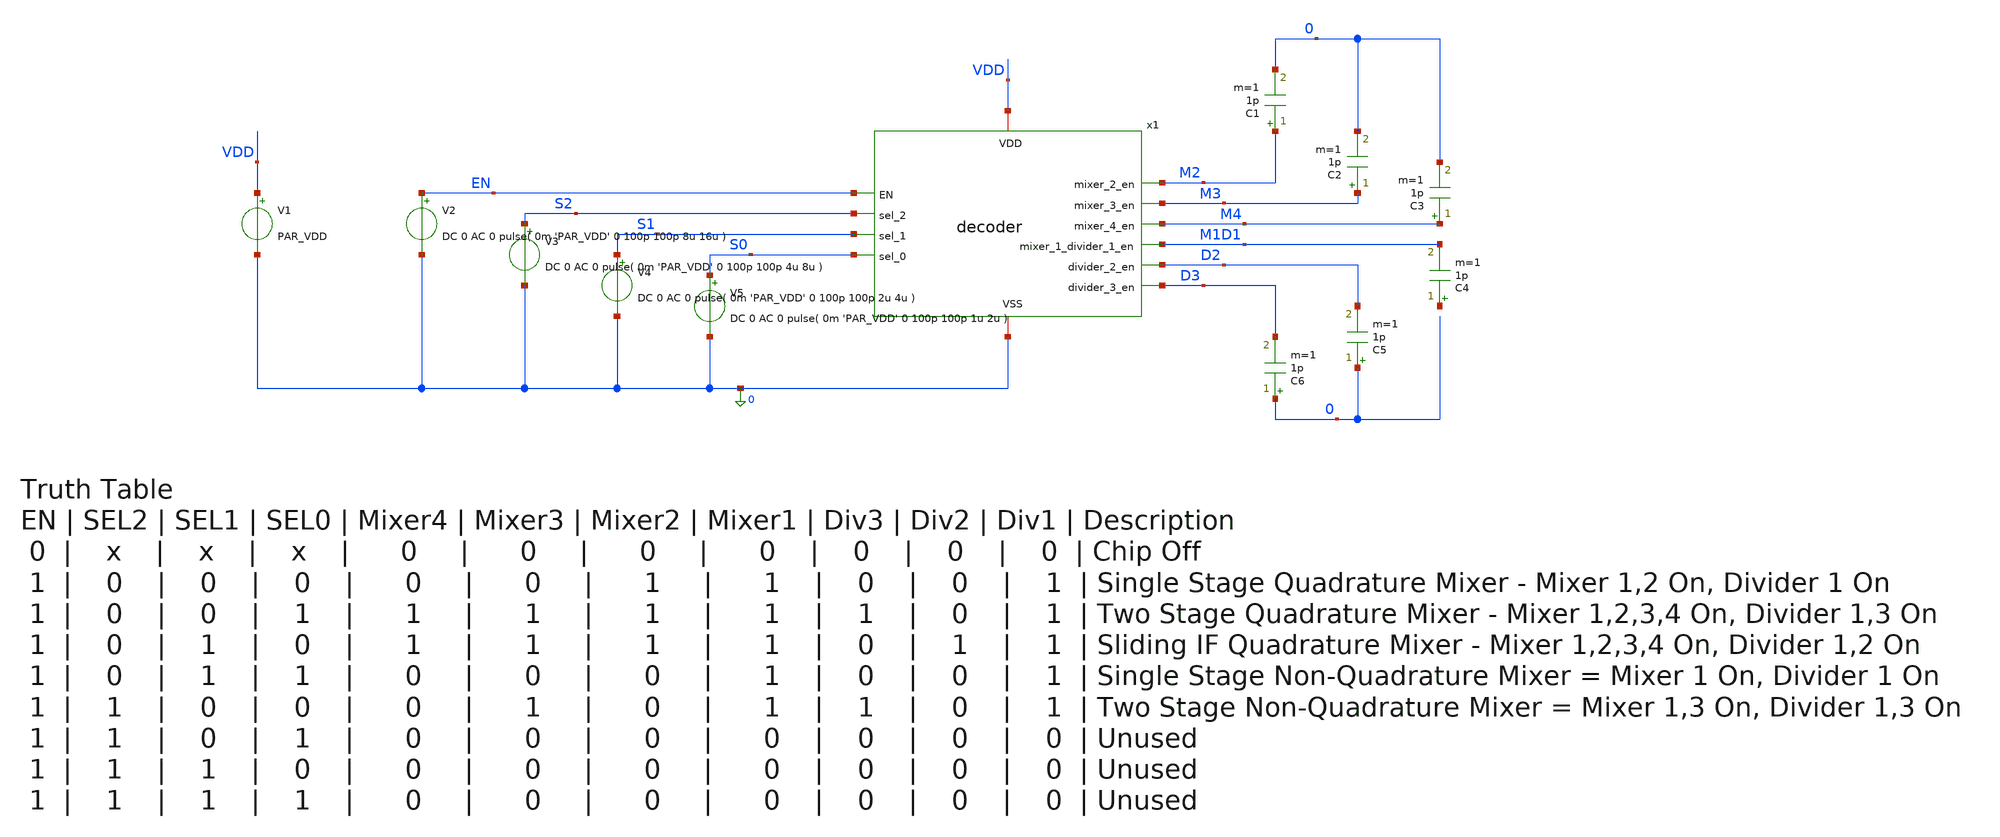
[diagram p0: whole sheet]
** sch_path: designs/decoder/testbench/tb_decoder.sch
**.subckt tb_decoder
C1 M2 0 1p m=1
C2 M3 0 1p m=1
C3 M4 0 1p m=1
C4 net1 M1D1 1p m=1
C5 0 D2 1p m=1
C6 0 D3 1p m=1
V1 VDD 0 PAR_VDD
V2 EN 0 DC 0 AC 0 pulse( 0m 'PAR_VDD' 0 100p 100p 8u 16u )
V3 S2 0 DC 0 AC 0 pulse( 0m 'PAR_VDD' 0 100p 100p 4u 8u )
V4 S1 0 DC 0 AC 0 pulse( 0m 'PAR_VDD' 0 100p 100p 2u 4u )
V5 S0 0 DC 0 AC 0 pulse( 0m 'PAR_VDD' 0 100p 100p 1u 2u )
x1 VDD 0 EN S2 M2 S1 M3 M4 S0 D2 D3 M1D1 decoder
**** begin user architecture code

.include $::180MCU_MODELS/design.ngspice
.lib $::180MCU_MODELS/sm141064.ngspice typical
.lib $::180MCU_MODELS/smbb000149.ngspice typical
.lib $::180MCU_MODELS/sm141064.ngspice cap_mim
.lib $::180MCU_MODELS/sm141064.ngspice res_typical
.lib $::180MCU_MODELS/sm141064.ngspice moscap_typical
.lib $::180MCU_MODELS/sm141064.ngspice mimcap_typical



** PARAMS

.PARAM PAR_VDD=3.3

.control
destroy all
save all
write tb_decoder.raw

tran 0.1u 16u

plot EN/3.3+3+.3 S2/3.3+2+.2 S1/3.3+1+.1 S0/3.3 M4/3.3+9+.9 M3/3.3+8+.8 M2/3.3+7+.7 M1D1/3.3+6+.6
+ D2/3.3+5+.5 D3/3.3+4+.4 nogrid
;plot x1.EN_BAR/3.3+3 x1.sel_2_bar/3.3+2 x1.sel_1_bar/3.3+1 x1.sel_0_bar/3.3

.endc


**** end user architecture code
**.ends
.end
